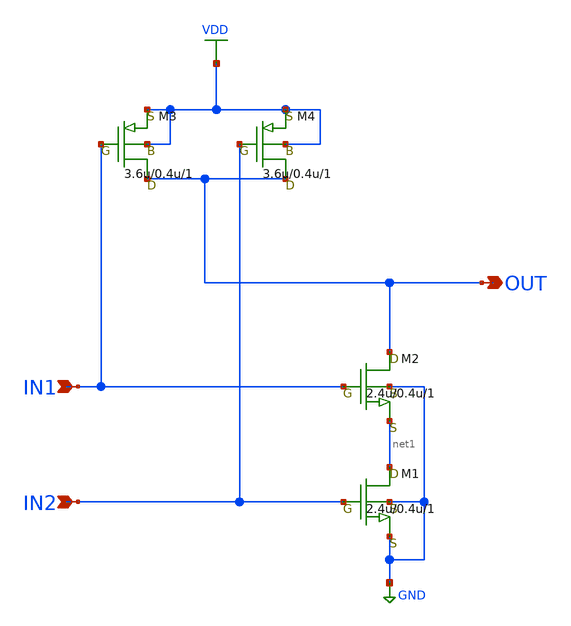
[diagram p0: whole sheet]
** sch_path: LR_hasegawa/LR_Work2/Citizen035/untitled.sch
**.subckt untitled IN1 IN2 OUT
*.ipin IN1
*.ipin IN2
*.opin OUT
M1 net1 IN2 GND GND nch w=2.4u l=0.4u as=0 ps=0 ad=0 pd=0 m=1
M2 OUT IN1 net1 GND nch w=2.4u l=0.4u as=0 ps=0 ad=0 pd=0 m=1
M3 OUT IN1 VDD VDD pch w=3.6u l=0.4u as=0 ps=0 ad=0 pd=0 m=1
M4 OUT IN2 VDD VDD pch w=3.6u l=0.4u as=0 ps=0 ad=0 pd=0 m=1
**.ends
.GLOBAL VDD
.GLOBAL GND
.end
